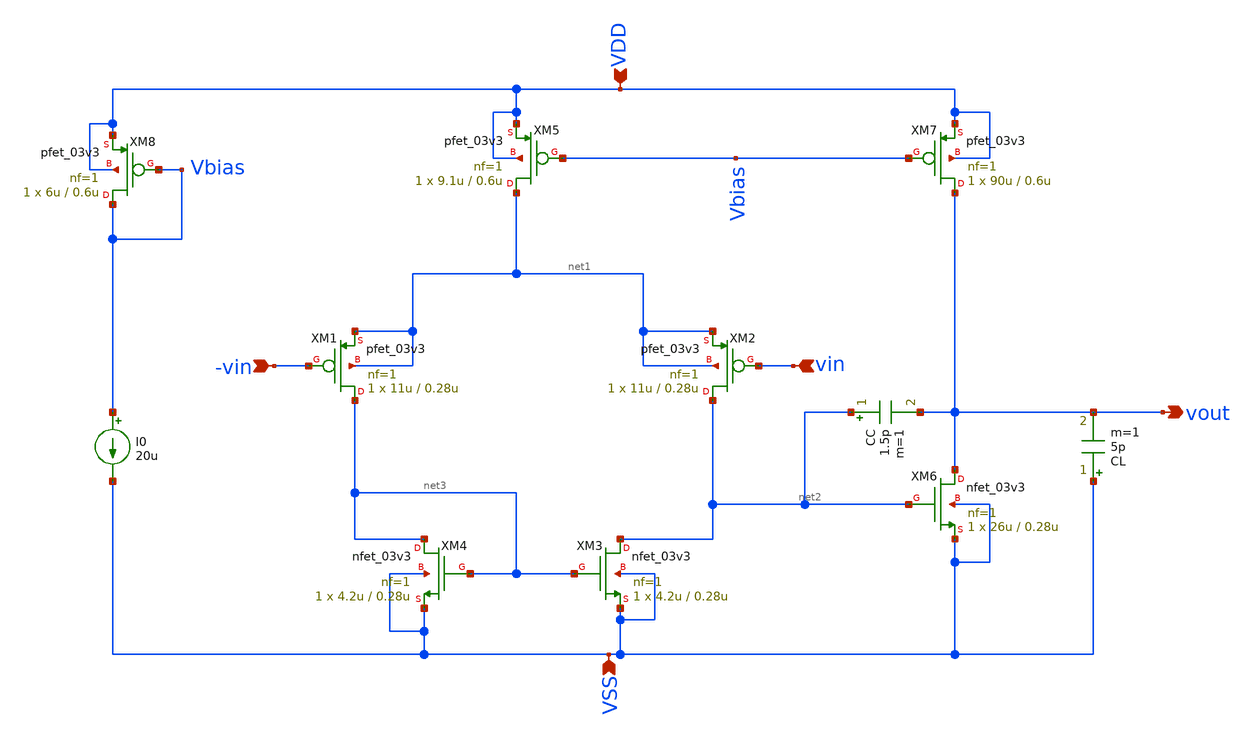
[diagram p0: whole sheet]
** sch_path: designs/OTApmosfinal.sch
**.subckt OTApmosfinal VDD VSS vin -vin vout
*.ipin VDD
*.ipin VSS
*.ipin vin
*.ipin -vin
*.opin vout
XM1 net3 -vin net1 net1 pfet_03v3 L=0.28u W=11u nf=1 ad='int((nf+1)/2) * W/nf * 0.18u' as='int((nf+2)/2) * W/nf * 0.18u'
+ pd='2*int((nf+1)/2) * (W/nf + 0.18u)' ps='2*int((nf+2)/2) * (W/nf + 0.18u)' nrd='0.18u / W' nrs='0.18u / W'
+ sa=0 sb=0 sd=0 m=1
XM2 net2 vin net1 net1 pfet_03v3 L=0.28u W=11u nf=1 ad='int((nf+1)/2) * W/nf * 0.18u' as='int((nf+2)/2) * W/nf * 0.18u'
+ pd='2*int((nf+1)/2) * (W/nf + 0.18u)' ps='2*int((nf+2)/2) * (W/nf + 0.18u)' nrd='0.18u / W' nrs='0.18u / W'
+ sa=0 sb=0 sd=0 m=1
XM5 net1 Vbias VDD VDD pfet_03v3 L=0.6u W=9.1u nf=1 ad='int((nf+1)/2) * W/nf * 0.18u' as='int((nf+2)/2) * W/nf * 0.18u'
+ pd='2*int((nf+1)/2) * (W/nf + 0.18u)' ps='2*int((nf+2)/2) * (W/nf + 0.18u)' nrd='0.18u / W' nrs='0.18u / W'
+ sa=0 sb=0 sd=0 m=1
XM4 net3 net3 VSS VSS nfet_03v3 L=0.28u W=4.2u nf=1 ad='int((nf+1)/2) * W/nf * 0.18u' as='int((nf+2)/2) * W/nf * 0.18u'
+ pd='2*int((nf+1)/2) * (W/nf + 0.18u)' ps='2*int((nf+2)/2) * (W/nf + 0.18u)' nrd='0.18u / W' nrs='0.18u / W'
+ sa=0 sb=0 sd=0 m=1
XM3 net2 net3 VSS VSS nfet_03v3 L=0.28u W=4.2u nf=1 ad='int((nf+1)/2) * W/nf * 0.18u' as='int((nf+2)/2) * W/nf * 0.18u'
+ pd='2*int((nf+1)/2) * (W/nf + 0.18u)' ps='2*int((nf+2)/2) * (W/nf + 0.18u)' nrd='0.18u / W' nrs='0.18u / W'
+ sa=0 sb=0 sd=0 m=1
XM6 vout net2 VSS VSS nfet_03v3 L=0.28u W=26u nf=1 ad='int((nf+1)/2) * W/nf * 0.18u' as='int((nf+2)/2) * W/nf * 0.18u'
+ pd='2*int((nf+1)/2) * (W/nf + 0.18u)' ps='2*int((nf+2)/2) * (W/nf + 0.18u)' nrd='0.18u / W' nrs='0.18u / W'
+ sa=0 sb=0 sd=0 m=1
XM7 vout Vbias VDD VDD pfet_03v3 L=0.6u W=90u nf=1 ad='int((nf+1)/2) * W/nf * 0.18u' as='int((nf+2)/2) * W/nf * 0.18u'
+ pd='2*int((nf+1)/2) * (W/nf + 0.18u)' ps='2*int((nf+2)/2) * (W/nf + 0.18u)' nrd='0.18u / W' nrs='0.18u / W'
+ sa=0 sb=0 sd=0 m=1
CC net2 vout 1.5p m=1
CL VSS vout 5p m=1
XM8 Vbias Vbias VDD VDD pfet_03v3 L=0.6u W=6u nf=1 ad='int((nf+1)/2) * W/nf * 0.18u' as='int((nf+2)/2) * W/nf * 0.18u'
+ pd='2*int((nf+1)/2) * (W/nf + 0.18u)' ps='2*int((nf+2)/2) * (W/nf + 0.18u)' nrd='0.18u / W' nrs='0.18u / W'
+ sa=0 sb=0 sd=0 m=1
I0 Vbias VSS 20u
**.ends
.end
